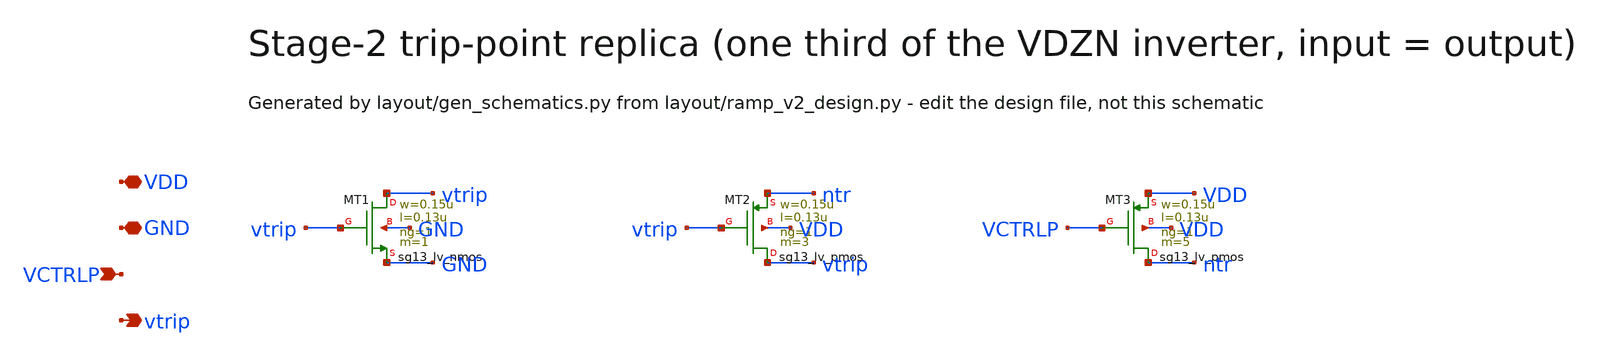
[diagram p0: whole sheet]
** sch_path: Design Files/RAMP/RAMP-V2/TRIP_V2.sch
**.subckt TRIP_V2 VDD GND VCTRLP vtrip
*.iopin VDD
*.iopin GND
*.ipin VCTRLP
*.opin vtrip
XMT1 vtrip vtrip GND GND sg13_lv_nmos w=0.15u l=0.13u ng=1 m=1 mm_ok=1
XMT2 vtrip vtrip ntr VDD sg13_lv_pmos w=0.15u l=0.13u ng=1 m=3 mm_ok=1
XMT3 ntr VCTRLP VDD VDD sg13_lv_pmos w=0.15u l=0.13u ng=1 m=5 mm_ok=1
**.ends
.end
